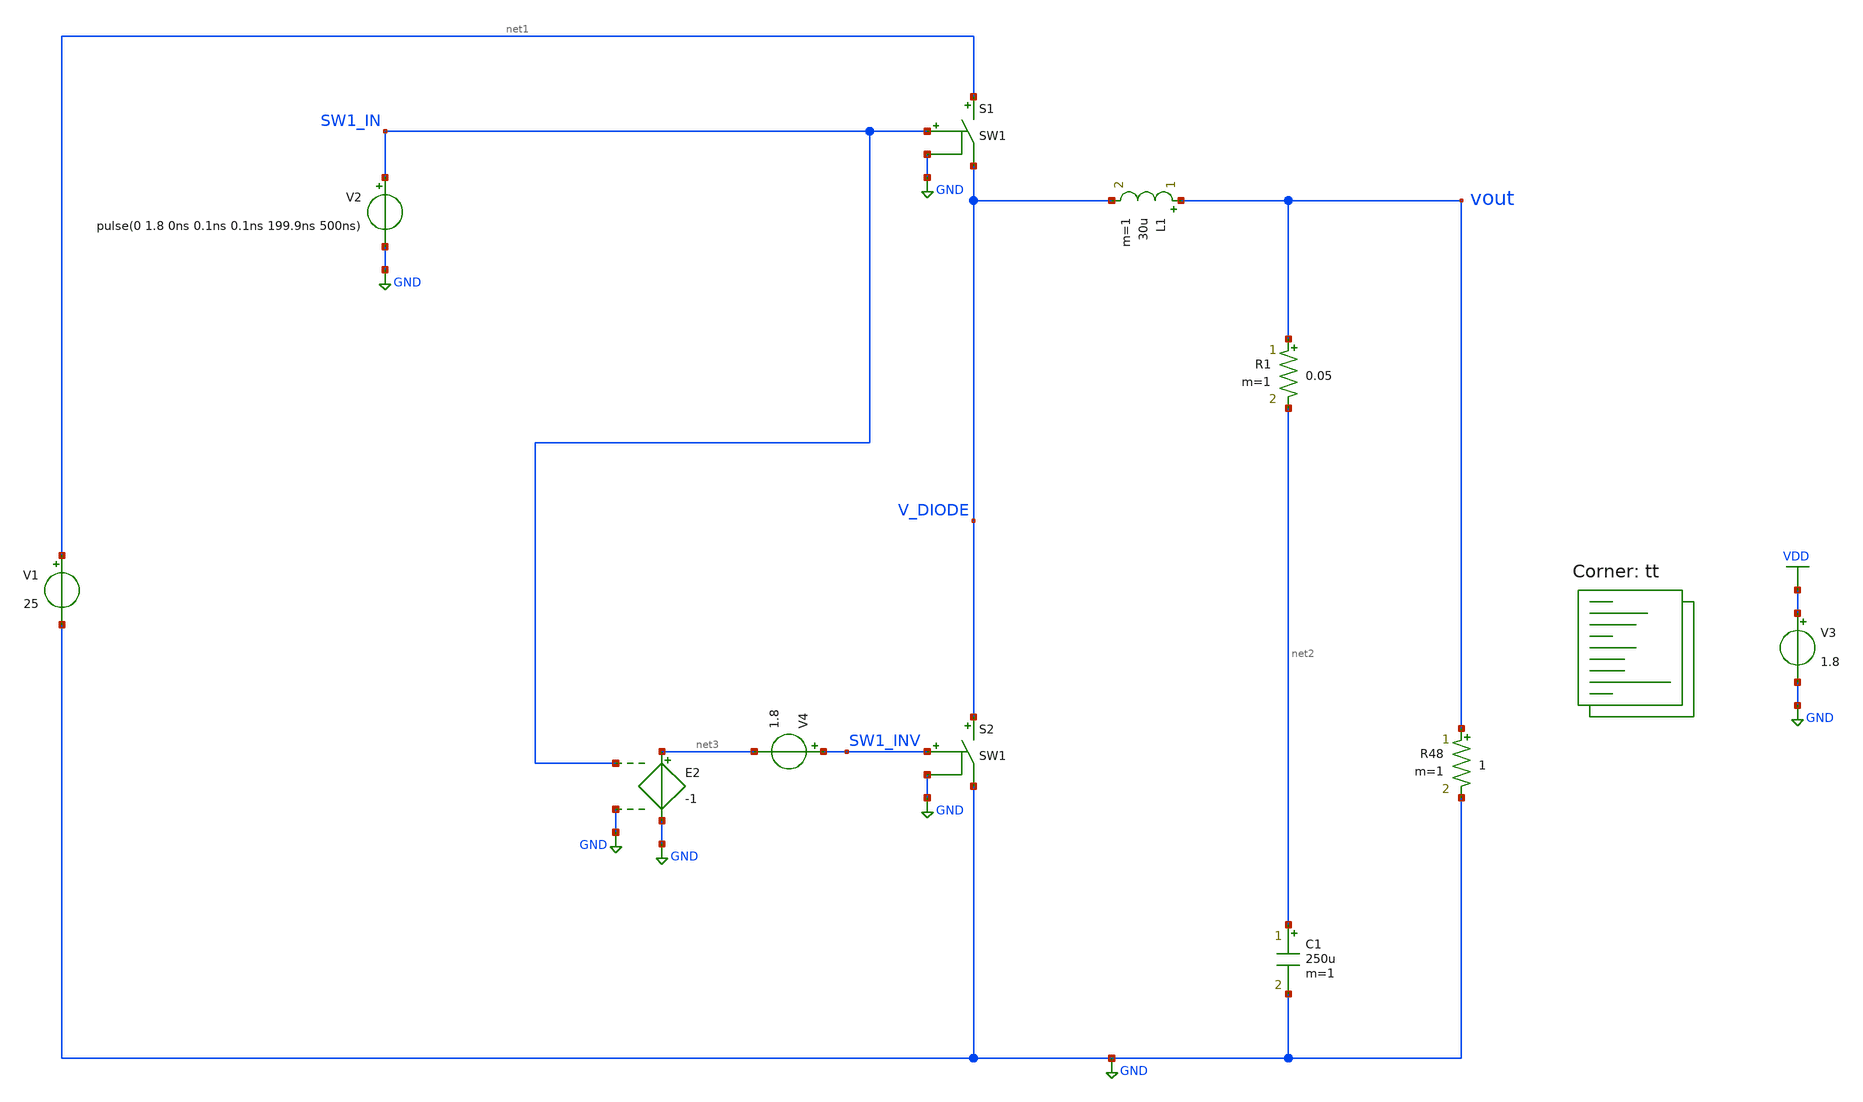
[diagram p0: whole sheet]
** sch_path: projects/ASU/EEE572/schematic/tb_buck_converter_6.sch
**.subckt tb_buck_converter_6
V1 net1 GND 25
R48 vout GND 1 m=1
L1 vout V_DIODE 30u m=1
C1 net2 GND 250u m=1
R1 vout net2 0.05 m=1
V2 SW1_IN GND pulse(0 1.8 0ns 0.1ns 0.1ns 199.9ns 500ns)
S1 net1 V_DIODE SW1_IN GND SW1
V3 VDD GND 1.8
S2 V_DIODE GND SW1_INV GND SW1
E2 net3 GND SW1_IN GND -1
V4 SW1_INV net3 1.8
**** begin user architecture code



.options method=gear
.options wnflag=1
.options savecurrents


* .model D1N914 D(Is=168.1E-21 N=1 Rs=.1 Ikf=1 Xti=3 Eg=1.11 Cjo=4p M=.3333 Vj=.75 Fc=.5 Bv=100
*+ Ibv=100u Tt=11.54n)
.model D1N914 D(Is=533.1E-6 N=1.95 Rs=0.00141 Cjo=1.34n M=0.333 Bv=35 Ibv=50u Tt=1.44n)


.control
  save all
  * save v(vout)
  * dc V1 0.0 2.0 0.005
  tran 100ns 3ms
  * tran 1ns 3ms
  remzerovec
  write tb_buck_converter_6.raw
  set appendwrite

.endc





.lib $::SKYWATER_MODELS/sky130.lib.spice tt
**** end user architecture code
**.ends
.GLOBAL GND
.GLOBAL VDD
**** begin user architecture code
.MODEL SW1 SW( VT=0.9 VH=0.01 RON=0.01 ROFF=10G )
**** end user architecture code
.end
